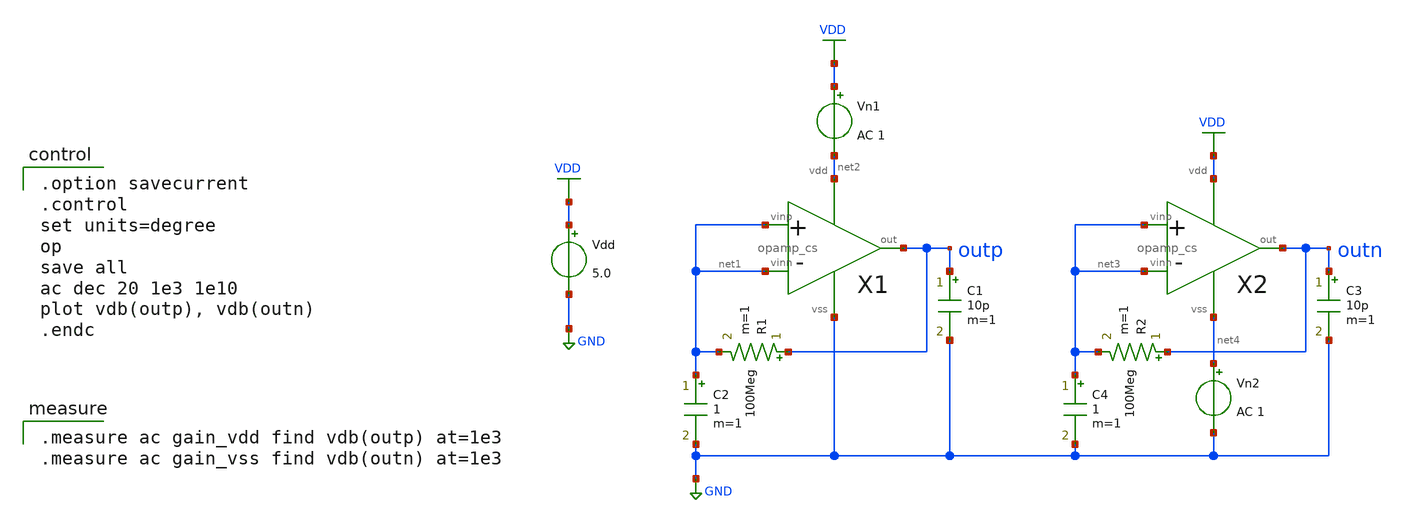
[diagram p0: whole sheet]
** sch_path: OR1/PTC06/opamp/opamp_cs_psrr.sch
**.subckt opamp_cs_psrr
Vdd VDD GND 5.0
C1 outp GND 10p m=1
R1 outp net1 100Meg m=1
C2 net1 GND 1 m=1
Vn1 VDD net2 AC 1
C3 outn GND 10p m=1
R2 outn net3 100Meg m=1
C4 net3 GND 1 m=1
Vn2 net4 GND AC 1
X1 net1 net1 outp net2 GND opamp_cs
X2 net3 net3 outn VDD net4 opamp_cs
**** begin user architecture code

.option savecurrent
.control
set units=degree
op
save all
ac dec 20 1e3 1e10
plot vdb(outp), vdb(outn)
.endc


.measure ac gain_vdd find vdb(outp) at=1e3
.measure ac gain_vss find vdb(outn) at=1e3

 .include $::LIB/mos.lib
.include $::LIB/passive.lib
.include $::LIB/diode.lib
**** end user architecture code
**.ends

* expanding   symbol:  opamp_cs.sym # of pins=5
** sym_path: OR1/PTC06/opamp/opamp_cs.sym
** sch_path: OR1/PTC06/opamp/opamp_cs.sch
.subckt opamp_cs vinp vinn out vdd vss
*.ipin vinp
*.ipin vinn
*.opin out
*.iopin vdd
*.iopin vss
X1 vinp vinn net2 vdd vss net5 diff
X2 net2 net5 out vdd vss cs
M3 net5 net5 vdd vdd pmos L=2u W=20u m=1
C1 out net3 poly_cap W=18 L=18
M2 net3 net1 net2 vss nmos L=2u W=40u m=1
M6 net1 net5 vdd vdd pmos L=2u W=20u m=1
M1 net1 net1 net4 vss nmos L=2u W=10u m=1
M7 net4 net4 vss vss nmos L=2u W=10u m=1
x3 vdd net7 vss cs-vth-ref_sym
M4 net6 net7 vdd vdd pmos L=2u W=20u m=1
M5 net6 net6 vss vss nmos L=2u W=5u m=1
M8 net5 net6 vss vss nmos L=2u W=5u m=1
.ends


* expanding   symbol:  diff.sym # of pins=6
** sym_path: diff.sym
** sch_path: diff.sch
.subckt diff vinp vinn out vdd vss vb
*.ipin vinn
*.ipin vinp
*.ipin vb
*.opin out
*.iopin vdd
*.iopin vss
M5 net2 vb vdd vdd pmos L=2u W=40u m=1
M1 net1 vinn net2 net2 pmos L=2u W=200u m=1
M2 out vinp net2 net2 pmos L=2u W=200u m=1
M3 net1 net1 vss vss nmos L=2u W=10u m=1
M4 out net1 vss vss nmos L=2u W=10u m=1
.ends


* expanding   symbol:  cs.sym # of pins=5
** sym_path: cs.sym
** sch_path: cs.sch
.subckt cs vin vb out vdd vss
*.ipin vb
*.ipin vin
*.opin out
*.iopin vss
*.iopin vdd
M6 out vb vdd vdd pmos L=2u W=400u m=1
M7 out vin vss vss nmos L=2u W=200u m=1
.ends


* expanding   symbol:  cs-vth-ref_sym.sym # of pins=3
** sym_path: cs-vth-ref_sym.sym
** sch_path: cs-vth-ref_sym.sch
.subckt cs-vth-ref_sym vdd ib vss
*.iopin vdd
*.iopin vss
*.iopin ib
R2 vss net2 HR_poly W=2.0 L=2000
M4 ib ib vdd vdd pmos L=2u W=100u m=1
M3 net1 ib vdd vdd pmos L=2u W=100u m=1
M2 ib net1 net2 vss nmos L=2u W=20u m=1
M1 net1 net2 vss vss nmos L=2u W=20u m=1
.ends

.GLOBAL GND
.GLOBAL VDD
.end
